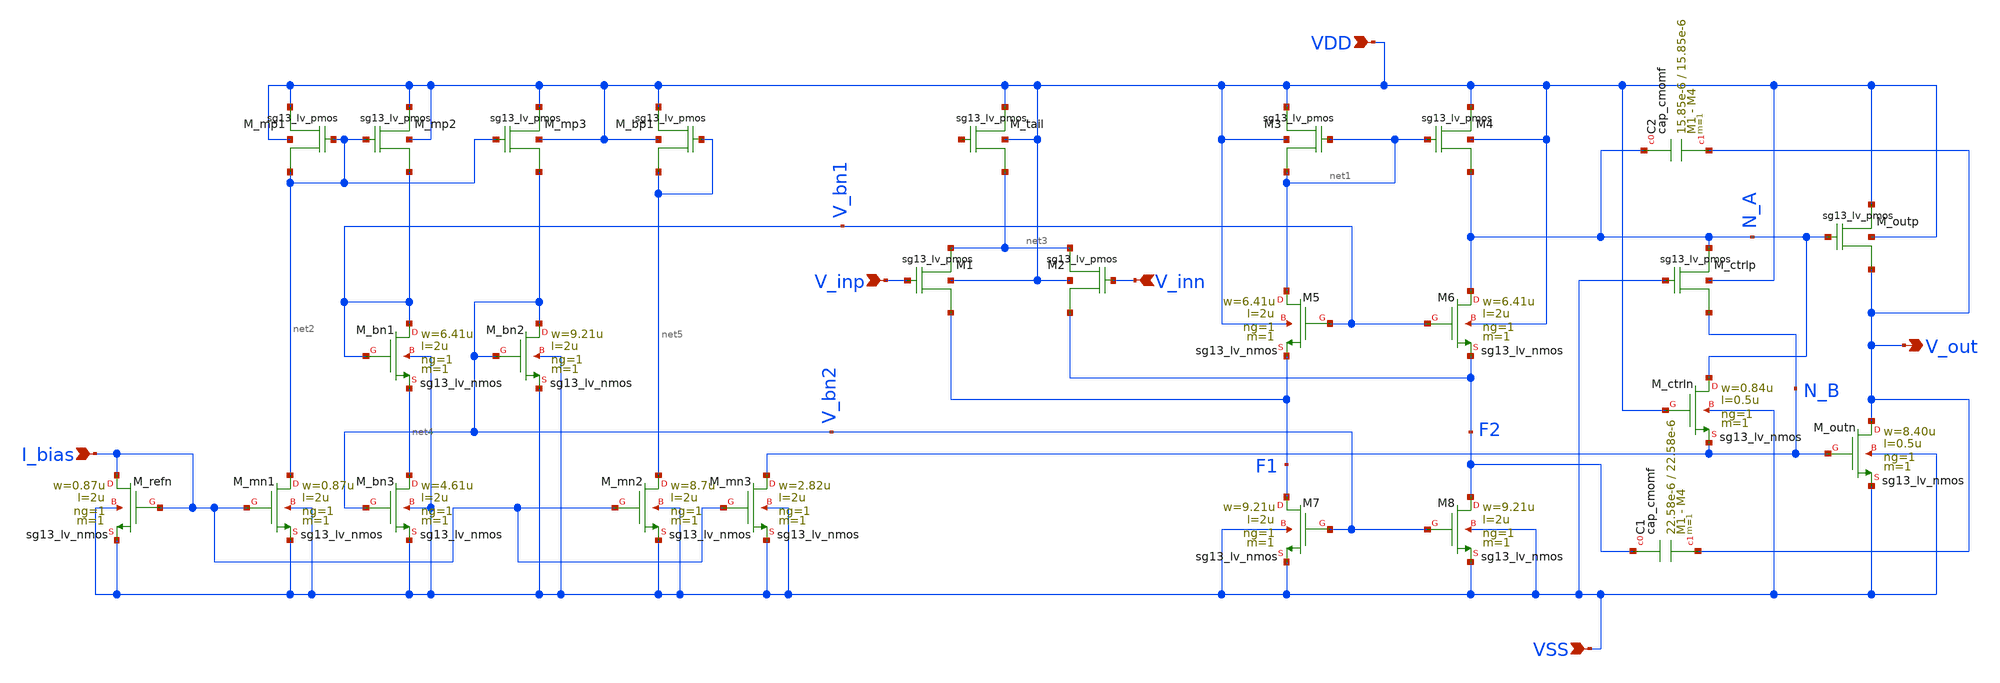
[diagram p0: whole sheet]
** sch_path: designs/libs/core_analog/coarse_gain/cg_ota.sch
**.subckt cg_ota V_inp VDD VSS V_out I_bias V_inn
*.ipin V_inp
*.ipin VDD
*.ipin VSS
*.opin V_out
*.ipin I_bias
*.ipin V_inn
XM1 net3 V_inp F1 VDD sg13_lv_pmos w=26.56u l=2u ng=4 m=1
XM2 net3 V_inn F2 VDD sg13_lv_pmos w=26.56u l=2u ng=4 m=1
XM3 VDD net1 net1 VDD sg13_lv_pmos w=7.33u l=2u ng=1 m=1
XM4 VDD net1 N_A VDD sg13_lv_pmos w=7.33u l=2u ng=1 m=1
XM7 F1 V_bn2 VSS VSS sg13_lv_nmos w=9.21u l=2u ng=1 m=1 mm_ok=1
XM8 F2 V_bn2 VSS VSS sg13_lv_nmos w=9.21u l=2u ng=1 m=1 mm_ok=1
XM_tail VDD net6 net3 VDD sg13_lv_pmos w=5.33u l=2u ng=1 m=4
XM_ctrlp N_A VSS N_B VDD sg13_lv_pmos w=2.20u l=0.50u ng=1 m=1
XM_outp VDD N_A V_out VDD sg13_lv_pmos w=22.20u l=0.5u ng=4 m=1
XM_ctrln N_A VDD N_B VSS sg13_lv_nmos w=0.84u l=0.5u ng=1 m=1 mm_ok=1
XM_outn V_out N_B VSS VSS sg13_lv_nmos w=8.40u l=0.5u ng=1 m=1 mm_ok=1
XC1 F2 V_out cap_cmomf w=22.58e-6 l=22.58e-6 mmin=1 mmax=4 subblock=0 rfmodel=0 subscale=1 m=1
+ mm_ok=1
XC2 N_A V_out cap_cmomf w=15.85e-6 l=15.85e-6 mmin=1 mmax=4 subblock=0 rfmodel=0 subscale=1 m=1
+ mm_ok=1
XM5 net1 V_bn1 F1 VDD sg13_lv_nmos w=6.41u l=2u ng=1 m=1 mm_ok=1
XM6 N_A V_bn1 F2 VDD sg13_lv_nmos w=6.41u l=2u ng=1 m=1 mm_ok=1
XM_mp1 VDD net2 net2 VDD sg13_lv_pmos w=2.30u l=2u ng=1 m=1
XM_mn1 net2 I_bias VSS VSS sg13_lv_nmos w=0.87u l=2u ng=1 m=1 mm_ok=1
XM_refn I_bias I_bias VSS VSS sg13_lv_nmos w=0.87u l=2u ng=1 m=1 mm_ok=1
XM_mp2 VDD net2 V_bn1 VDD sg13_lv_pmos w=11.50u l=2u ng=2 m=1
XM_mp3 VDD net2 V_bn2 VDD sg13_lv_pmos w=22.30u l=2u ng=4 m=1
XM_bn1 V_bn1 V_bn1 net4 VSS sg13_lv_nmos w=6.41u l=2u ng=1 m=1 mm_ok=1
XM_bn2 V_bn2 V_bn2 VSS VSS sg13_lv_nmos w=9.21u l=2u ng=1 m=1 mm_ok=1
XM_bn3 net4 V_bn2 VSS VSS sg13_lv_nmos w=4.61u l=2u ng=1 m=1 mm_ok=1
XM_mn2 net5 I_bias VSS VSS sg13_lv_nmos w=8.7u l=2u ng=1 m=1 mm_ok=1
XM_bp1 VDD net5 net5 VDD sg13_lv_pmos w=5.33u l=2u ng=1 m=4
XM_mn3 N_B I_bias VSS VSS sg13_lv_nmos w=2.82u l=2u ng=1 m=1 mm_ok=1
**.ends
.end
